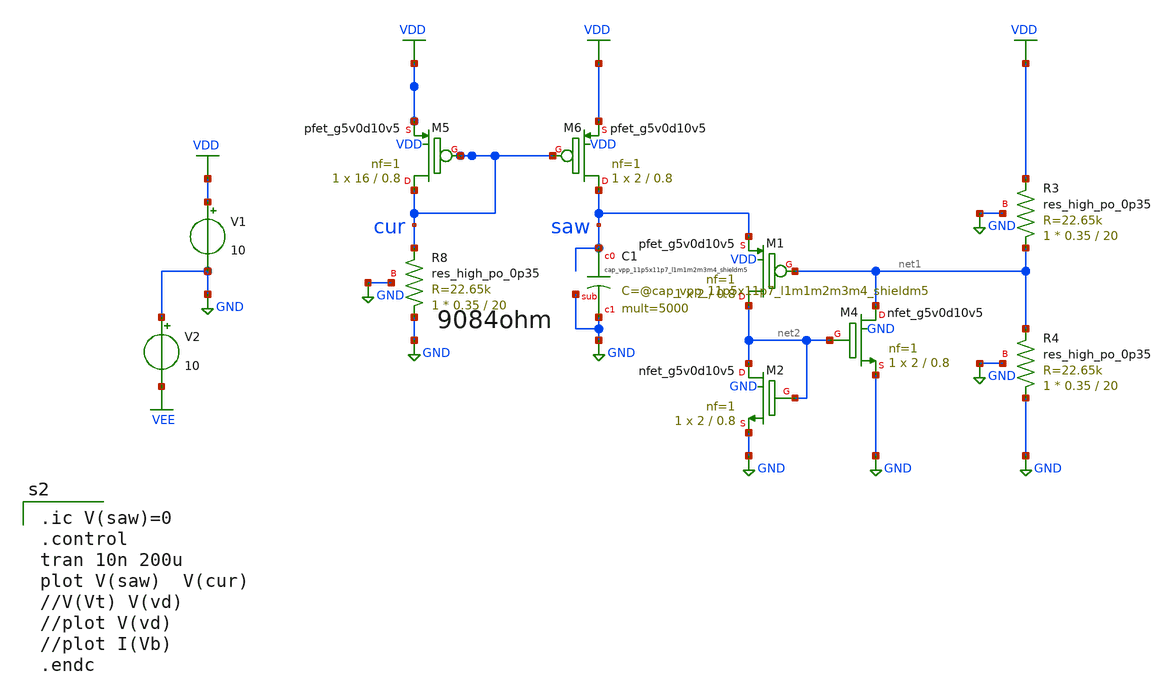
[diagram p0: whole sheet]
** sch_path: xschem/sawgen-fet-sky130.sch
**.subckt sawgen-fet-sky130
V1 VDD GND 10
V2 GND VEE 10
XM5 cur cur VDD VDD sky130_fd_pr__pfet_g5v0d10v5 L=0.8 W=16 nf=1 ad='int((nf+1)/2) * W/nf * 0.29' as='int((nf+2)/2) * W/nf * 0.29'
+ pd='2*int((nf+1)/2) * (W/nf + 0.29)' ps='2*int((nf+2)/2) * (W/nf + 0.29)' nrd='0.29 / W' nrs='0.29 / W'
+ sa=0 sb=0 sd=0 mult=1 m=1
XM6 saw cur VDD VDD sky130_fd_pr__pfet_g5v0d10v5 L=0.8 W=2 nf=1 ad='int((nf+1)/2) * W/nf * 0.29' as='int((nf+2)/2) * W/nf * 0.29'
+ pd='2*int((nf+1)/2) * (W/nf + 0.29)' ps='2*int((nf+2)/2) * (W/nf + 0.29)' nrd='0.29 / W' nrs='0.29 / W'
+ sa=0 sb=0 sd=0 mult=1 m=1
XR8 GND cur GND sky130_fd_pr__res_high_po_0p35 L=20 mult=1 m=1
XM1 net2 net1 saw VDD sky130_fd_pr__pfet_g5v0d10v5 L=0.8 W=2 nf=1 ad='int((nf+1)/2) * W/nf * 0.29' as='int((nf+2)/2) * W/nf * 0.29'
+ pd='2*int((nf+1)/2) * (W/nf + 0.29)' ps='2*int((nf+2)/2) * (W/nf + 0.29)' nrd='0.29 / W' nrs='0.29 / W'
+ sa=0 sb=0 sd=0 mult=1 m=1
XM2 net2 net2 GND GND sky130_fd_pr__nfet_g5v0d10v5 L=0.8 W=2 nf=1 ad='int((nf+1)/2) * W/nf * 0.29' as='int((nf+2)/2) * W/nf * 0.29'
+ pd='2*int((nf+1)/2) * (W/nf + 0.29)' ps='2*int((nf+2)/2) * (W/nf + 0.29)' nrd='0.29 / W' nrs='0.29 / W'
+ sa=0 sb=0 sd=0 mult=1 m=1
XM4 net1 net2 GND GND sky130_fd_pr__nfet_g5v0d10v5 L=0.8 W=2 nf=1 ad='int((nf+1)/2) * W/nf * 0.29' as='int((nf+2)/2) * W/nf * 0.29'
+ pd='2*int((nf+1)/2) * (W/nf + 0.29)' ps='2*int((nf+2)/2) * (W/nf + 0.29)' nrd='0.29 / W' nrs='0.29 / W'
+ sa=0 sb=0 sd=0 mult=1 m=1
XR3 net1 VDD GND sky130_fd_pr__res_high_po_0p35 L=20 mult=1 m=1
XR4 GND net1 GND sky130_fd_pr__res_high_po_0p35 L=20 mult=1 m=1
XC1 saw GND GND sky130_fd_pr__cap_vpp_11p5x11p7_l1m1m2m3m4_shieldm5 mult=5000 m=5000
**** begin user architecture code


.model BSS84 VDMOS(pchan Rg=3 Vto=-2.1 Rd=2.4 Rs=1.8 Rb=3 Kp=.2 Cgdmax=.04n Cgdmin=.001n Cgs=.02n
+ Cjo=.01n Is=2p mfg=Philips Vds=-50 Ron=6000m Qg=1n)
.model 2N7002 VDMOS(Rg=3 Vto=1.6 Rd=0 Rs=.75 Rb=.14 Kp=.17 mtriode=1.25 Cgdmax=80p Cgdmin=12p
+ Cgs=50p Cjo=50p Is=.04p mfg=Fairchild Vds=60 Ron=2 Qg=1.5n)


.model 2N3904 NPN(IS=1E-14 VAF=100   Bf=300 IKF=0.4 XTB=1.5 BR=4   CJC=4E-12  CJE=8E-12 RB=20 RC=0.1
+ RE=0.1   TR=250E-9  TF=350E-12 ITF=1 VTF=2 XTF=3 Vceo=40 Icrating=200m mfg=Philips)

.model 2N3906 PNP(IS=1E-14 VAF=100   BF=200 IKF=0.4 XTB=1.5 BR=4   CJC=4.5E-12 CJE=10E-12 RB=20
+ RC=0.1 RE=0.1   TR=250E-9   TF=350E-12 ITF=1 VTF=2 XTF=3 Vceo=40  Icrating=200m mfg=Philips)

//.include /usr/share/pdk/sky130A/libs.ref/sky130_fd_pr/spice/sky130_fd_pr__nfet_g5v0d10v5.pm3.spice
//.include /usr/share/pdk/sky130A/libs.ref/sky130_fd_pr/spice/sky130_fd_pr__res_high_po_0p35.model.spice

.lib /usr/share/pdk/sky130A/libs.tech/ngspice/sky130.lib.spice tt
.include /usr/share/pdk/sky130A/libs.ref/sky130_fd_sc_hvl/spice/sky130_fd_sc_hvl.spice


.ic V(saw)=0
.control
tran 10n 200u
plot V(saw)  V(cur)
//V(Vt) V(vd)
//plot V(vd)
//plot I(Vb)
.endc

**** end user architecture code
**.ends
.GLOBAL VDD
.GLOBAL GND
.GLOBAL VEE
.end
